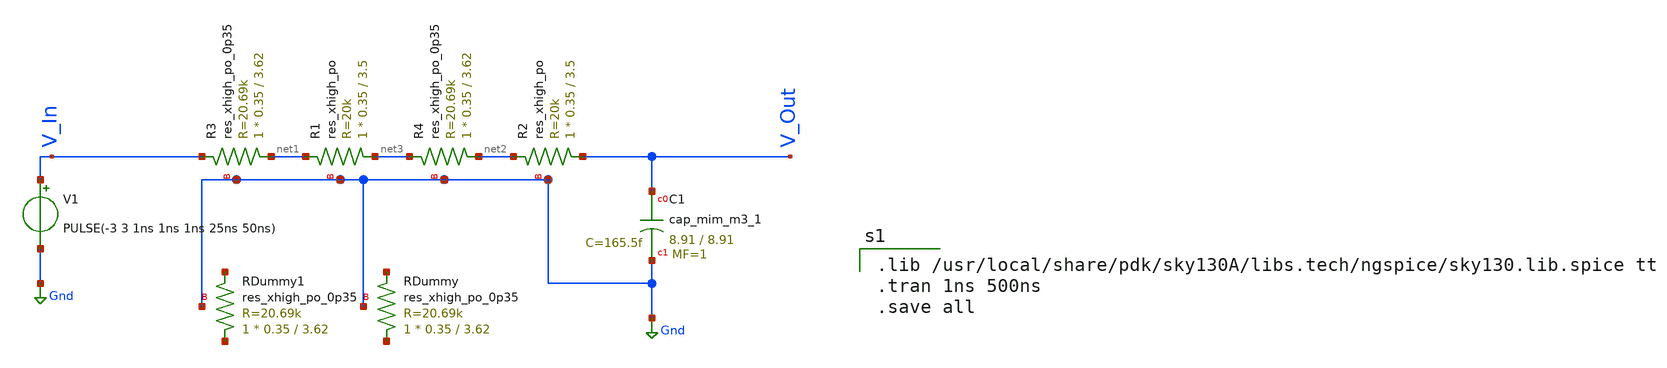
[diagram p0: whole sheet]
** sch_path: Schematic/RC-lowPassFilter/RC-LowPassFilter.sch
**.subckt RC-LowPassFilter
XR1 net3 net1 Gnd sky130_fd_pr__res_xhigh_po W=0.35 L=3.5 mult=1 m=1
XR3 net1 V_In Gnd sky130_fd_pr__res_xhigh_po_0p35 L=3.62 mult=1 m=1
XR2 V_Out net2 Gnd sky130_fd_pr__res_xhigh_po W=0.35 L=3.5 mult=1 m=1
XR4 net2 net3 Gnd sky130_fd_pr__res_xhigh_po_0p35 L=3.62 mult=1 m=1
XC1 V_Out Gnd sky130_fd_pr__cap_mim_m3_1 W=8.91 L=8.91 MF=1 m=1
XRDummy1 net4 net5 Gnd sky130_fd_pr__res_xhigh_po_0p35 L=3.62 mult=1 m=1
XRDummy net6 net7 Gnd sky130_fd_pr__res_xhigh_po_0p35 L=3.62 mult=1 m=1
V1 V_In Gnd PULSE(-3 3 1ns 1ns 1ns 25ns 50ns)
**** begin user architecture code

.lib /usr/local/share/pdk/sky130A/libs.tech/ngspice/sky130.lib.spice tt
.tran 1ns 500ns
.save all


**** end user architecture code
**.ends
.GLOBAL Gnd
.end
